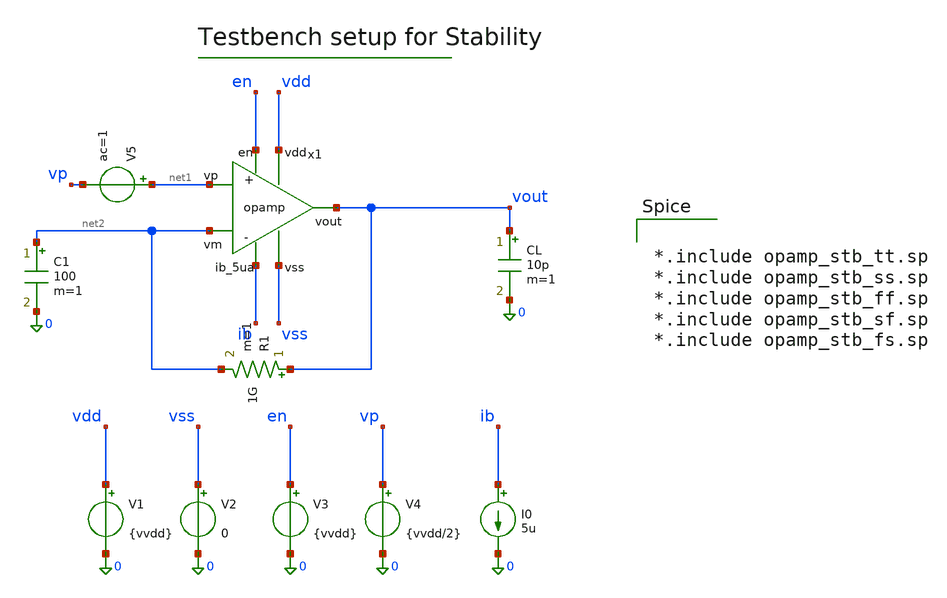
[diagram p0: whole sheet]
** sch_path: xschem/opamp/sim_opamp_stb.sch
**.subckt sim_opamp_stb
x1 vdd vss vout net1 net2 ib en opamp
V1 vdd 0 {vvdd}
V2 vss 0 0
V3 en 0 {vvdd}
V4 vp 0 {vvdd/2}
I0 ib 0 5u
CL vout 0 10p m=1
R1 vout net2 1G m=1
C1 net2 0 100 m=1
V5 net1 vp ac=1
**** begin user architecture code


*.include opamp_stb_tt.sp
*.include opamp_stb_ss.sp
*.include opamp_stb_ff.sp
*.include opamp_stb_sf.sp
*.include opamp_stb_fs.sp


**** end user architecture code
**.ends

* expanding   symbol:  opamp.sym # of pins=7
** sym_path: xschem/opamp/opamp.sym
** sch_path: xschem/opamp/opamp.sch
.subckt opamp vdd vss vout vp vm ib_5ua en
*.ipin vdd
*.ipin vss
*.ipin vm
*.ipin vp
*.ipin ib_5ua
*.opin vout
*.ipin en
XM1 net2 vm net1 vdd sky130_fd_pr__pfet_01v8_lvt L=0.5 W=25 nf=5 ad='int((5 + 1)/2) * 25 / 5 * 0.29'
+ as='int((5 + 2)/2) * 25 / 5 * 0.29' pd='2*int((5 + 1)/2) * (25 / 5 + 0.29)' ps='2*int((5 + 2)/2) * (25 / 5 + 0.29)'
+ nrd='0.29 / 25 ' nrs='0.29 / 25 ' sa=0 sb=0 sd=0 mult=1 m=1
XM2 net3 vp net1 vdd sky130_fd_pr__pfet_01v8_lvt L=0.5 W=25 nf=5 ad='int((5 + 1)/2) * 25 / 5 * 0.29'
+ as='int((5 + 2)/2) * 25 / 5 * 0.29' pd='2*int((5 + 1)/2) * (25 / 5 + 0.29)' ps='2*int((5 + 2)/2) * (25 / 5 + 0.29)'
+ nrd='0.29 / 25 ' nrs='0.29 / 25 ' sa=0 sb=0 sd=0 mult=1 m=1
XM3 net2 net2 vss vss sky130_fd_pr__nfet_01v8_lvt L=1 W=0.7 nf=1 ad='int((1 + 1)/2) * 0.7 / 1 * 0.29'
+ as='int((1 + 2)/2) * 0.7 / 1 * 0.29' pd='2*int((1 + 1)/2) * (0.7 / 1 + 0.29)' ps='2*int((1 + 2)/2) * (0.7 / 1 + 0.29)'
+ nrd='0.29 / 0.7 ' nrs='0.29 / 0.7 ' sa=0 sb=0 sd=0 mult=1 m=1
XM4 net3 net2 vss vss sky130_fd_pr__nfet_01v8_lvt L=1 W=0.7 nf=1 ad='int((1 + 1)/2) * 0.7 / 1 * 0.29'
+ as='int((1 + 2)/2) * 0.7 / 1 * 0.29' pd='2*int((1 + 1)/2) * (0.7 / 1 + 0.29)' ps='2*int((1 + 2)/2) * (0.7 / 1 + 0.29)'
+ nrd='0.29 / 0.7 ' nrs='0.29 / 0.7 ' sa=0 sb=0 sd=0 mult=1 m=1
XM5 net1 net4 vdd vdd sky130_fd_pr__pfet_01v8_lvt L=1 W=12 nf=2 ad='int((2 + 1)/2) * 12 / 2 * 0.29' as='int((2 + 2)/2) * 12 / 2 * 0.29'
+ pd='2*int((2 + 1)/2) * (12 / 2 + 0.29)' ps='2*int((2 + 2)/2) * (12 / 2 + 0.29)' nrd='0.29 / 12 ' nrs='0.29 / 12 '
+ sa=0 sb=0 sd=0 mult=1 m=1
XM6 vout net3 vss vss sky130_fd_pr__nfet_01v8_lvt L=0.6 W=10 nf=2 ad='int((2 + 1)/2) * 10 / 2 * 0.29'
+ as='int((2 + 2)/2) * 10 / 2 * 0.29' pd='2*int((2 + 1)/2) * (10 / 2 + 0.29)' ps='2*int((2 + 2)/2) * (10 / 2 + 0.29)'
+ nrd='0.29 / 10 ' nrs='0.29 / 10 ' sa=0 sb=0 sd=0 mult=1 m=1
XM7 vout net4 vdd vdd sky130_fd_pr__pfet_01v8_lvt L=1 W=72 nf=12 ad='int((12 + 1)/2) * 72 / 12 * 0.29'
+ as='int((12 + 2)/2) * 72 / 12 * 0.29' pd='2*int((12 + 1)/2) * (72 / 12 + 0.29)' ps='2*int((12 + 2)/2) * (72 / 12 + 0.29)'
+ nrd='0.29 / 72 ' nrs='0.29 / 72 ' sa=0 sb=0 sd=0 mult=1 m=1
XM8 net4 net4 vdd vdd sky130_fd_pr__pfet_01v8_lvt L=1 W=6 nf=1 ad='int((1 + 1)/2) * 6 / 1 * 0.29' as='int((1 + 2)/2) * 6 / 1 * 0.29'
+ pd='2*int((1 + 1)/2) * (6 / 1 + 0.29)' ps='2*int((1 + 2)/2) * (6 / 1 + 0.29)' nrd='0.29 / 6 ' nrs='0.29 / 6 '
+ sa=0 sb=0 sd=0 mult=1 m=1
XM9 net4 en vdd vdd sky130_fd_pr__pfet_01v8_lvt L=1 W=1 nf=1 ad='int((1 + 1)/2) * 1 / 1 * 0.29' as='int((1 + 2)/2) * 1 / 1 * 0.29'
+ pd='2*int((1 + 1)/2) * (1 / 1 + 0.29)' ps='2*int((1 + 2)/2) * (1 / 1 + 0.29)' nrd='0.29 / 1 ' nrs='0.29 / 1 '
+ sa=0 sb=0 sd=0 mult=1 m=1
XM10 net2 enb vss vss sky130_fd_pr__nfet_01v8_lvt L=1 W=1 nf=1 ad='int((1 + 1)/2) * 1 / 1 * 0.29' as='int((1 + 2)/2) * 1 / 1 * 0.29'
+ pd='2*int((1 + 1)/2) * (1 / 1 + 0.29)' ps='2*int((1 + 2)/2) * (1 / 1 + 0.29)' nrd='0.29 / 1 ' nrs='0.29 / 1 '
+ sa=0 sb=0 sd=0 mult=1 m=1
XM11 net3 enb vss vss sky130_fd_pr__nfet_01v8_lvt L=1 W=1 nf=1 ad='int((1 + 1)/2) * 1 / 1 * 0.29' as='int((1 + 2)/2) * 1 / 1 * 0.29'
+ pd='2*int((1 + 1)/2) * (1 / 1 + 0.29)' ps='2*int((1 + 2)/2) * (1 / 1 + 0.29)' nrd='0.29 / 1 ' nrs='0.29 / 1 '
+ sa=0 sb=0 sd=0 mult=1 m=1
XM12 ib_5ua enb net4 vdd sky130_fd_pr__pfet_01v8_lvt L=0.35 W=1 nf=2 ad='int((2 + 1)/2) * 1 / 2 * 0.29'
+ as='int((2 + 2)/2) * 1 / 2 * 0.29' pd='2*int((2 + 1)/2) * (1 / 2 + 0.29)' ps='2*int((2 + 2)/2) * (1 / 2 + 0.29)'
+ nrd='0.29 / 1 ' nrs='0.29 / 1 ' sa=0 sb=0 sd=0 mult=1 m=1
x1 vdd en enb vss inv
XCC[9] net3 vout sky130_fd_pr__cap_mim_m3_2 W=10 L=10 MF=1 m=1
XCC[8] net3 vout sky130_fd_pr__cap_mim_m3_2 W=10 L=10 MF=1 m=1
XCC[7] net3 vout sky130_fd_pr__cap_mim_m3_2 W=10 L=10 MF=1 m=1
XCC[6] net3 vout sky130_fd_pr__cap_mim_m3_2 W=10 L=10 MF=1 m=1
XCC[5] net3 vout sky130_fd_pr__cap_mim_m3_2 W=10 L=10 MF=1 m=1
XCC[4] net3 vout sky130_fd_pr__cap_mim_m3_2 W=10 L=10 MF=1 m=1
XCC[3] net3 vout sky130_fd_pr__cap_mim_m3_2 W=10 L=10 MF=1 m=1
XCC[2] net3 vout sky130_fd_pr__cap_mim_m3_2 W=10 L=10 MF=1 m=1
XCC[1] net3 vout sky130_fd_pr__cap_mim_m3_2 W=10 L=10 MF=1 m=1
XCC[0] net3 vout sky130_fd_pr__cap_mim_m3_2 W=10 L=10 MF=1 m=1
.ends


* expanding   symbol:  /home/guru/Projects/sky130_opamp/xschem/inv/inv.sym # of pins=4
** sym_path: xschem/inv/inv.sym
** sch_path: xschem/inv/inv.sch
.subckt inv vdd x y vss
*.ipin vdd
*.ipin vss
*.ipin x
*.opin y
XM1 y x vdd vdd sky130_fd_pr__pfet_01v8_lvt L=0.5 W=1.2 nf=1 ad='int((1 + 1)/2) * 1.2 / 1 * 0.29' as='int((1 + 2)/2) * 1.2 / 1 * 0.29'
+ pd='2*int((1 + 1)/2) * (1.2 / 1 + 0.29)' ps='2*int((1 + 2)/2) * (1.2 / 1 + 0.29)' nrd='0.29 / 1.2 ' nrs='0.29 / 1.2 '
+ sa=0 sb=0 sd=0 mult=1 m=1
XM2 y x vss vss sky130_fd_pr__nfet_01v8_lvt L=0.5 W=0.5 nf=1 ad='int((1 + 1)/2) * 0.5 / 1 * 0.29' as='int((1 + 2)/2) * 0.5 / 1 * 0.29'
+ pd='2*int((1 + 1)/2) * (0.5 / 1 + 0.29)' ps='2*int((1 + 2)/2) * (0.5 / 1 + 0.29)' nrd='0.29 / 0.5 ' nrs='0.29 / 0.5 '
+ sa=0 sb=0 sd=0 mult=1 m=1
.ends

.end
